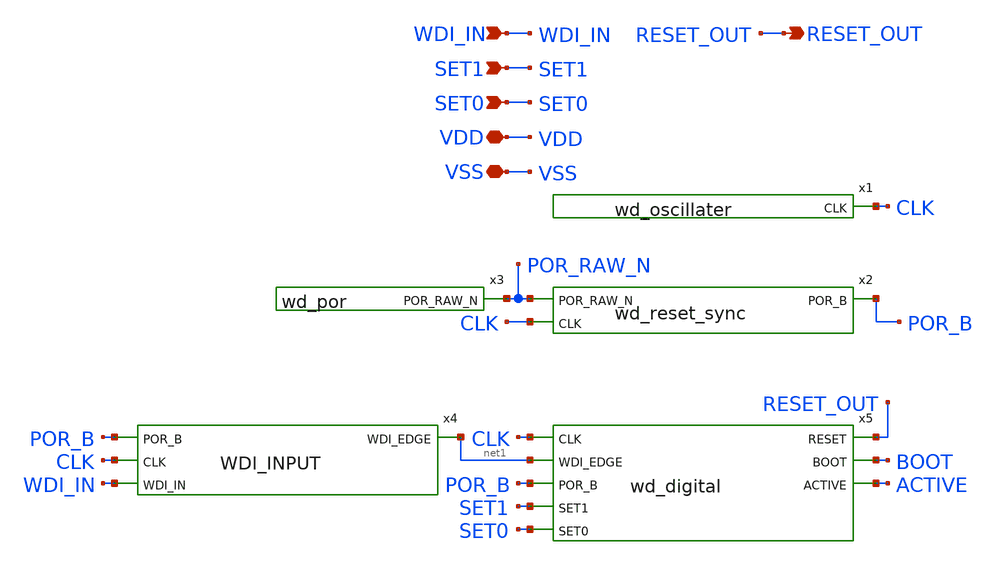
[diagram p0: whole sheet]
** sch_path: design/top/schematic/wd_watchdog.sch
**.subckt wd_watchdog SET1 SET0 WDI_IN RESET_OUT VDD VSS
*.ipin SET1
*.ipin SET0
*.ipin WDI_IN
*.opin RESET_OUT
*.iopin VDD
*.iopin VSS
x1 CLK VDD VSS wd_oscillater
x2 POR_RAW_N CLK POR_B VDD VSS wd_reset_sync
x3 POR_RAW_N VDD VSS wd_por
x4 POR_B CLK WDI_IN net1 VDD VSS WDI_INPUT
x5 RESET_OUT BOOT CLK net1 ACTIVE POR_B SET1 SET0 VDD VSS wd_digital
**.ends
.end
